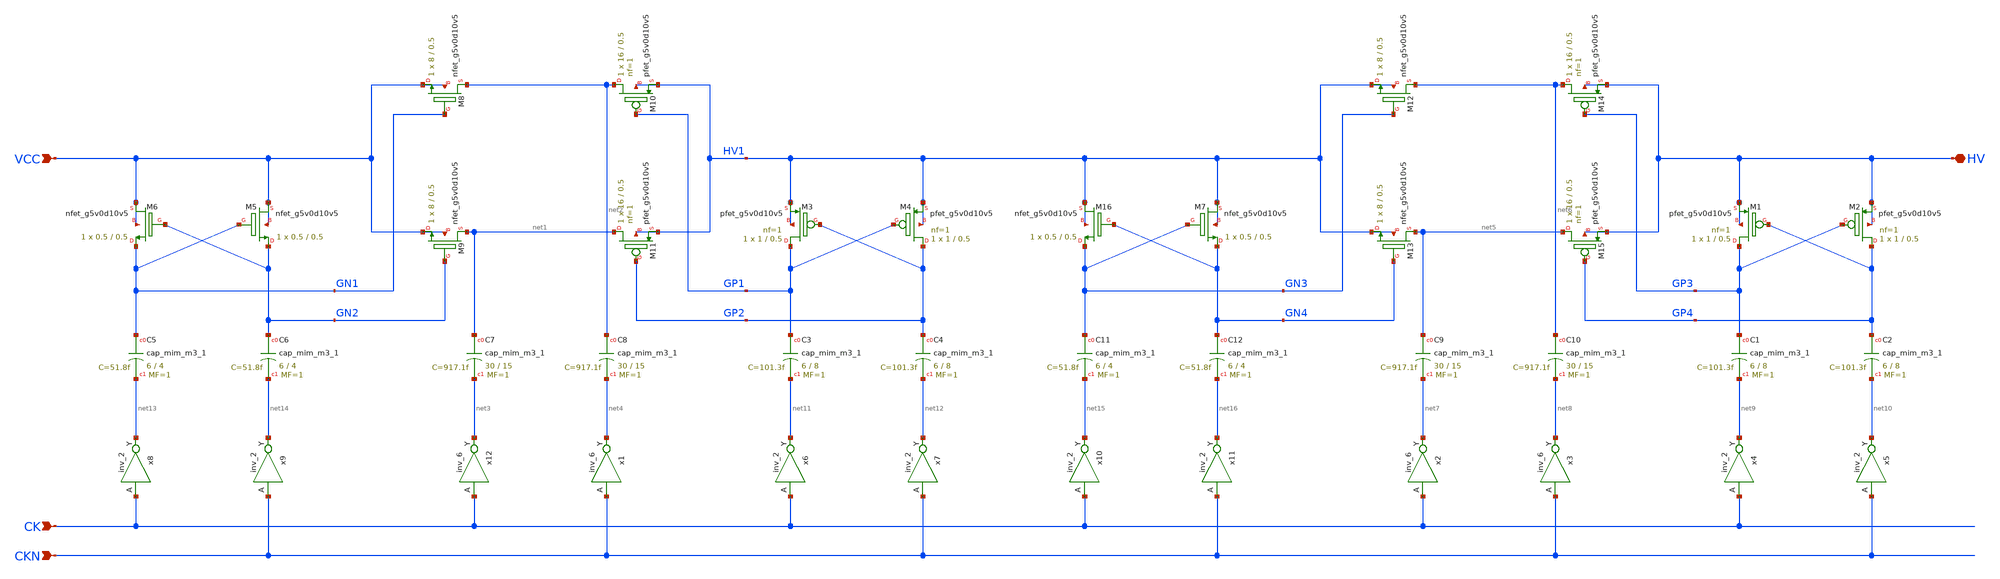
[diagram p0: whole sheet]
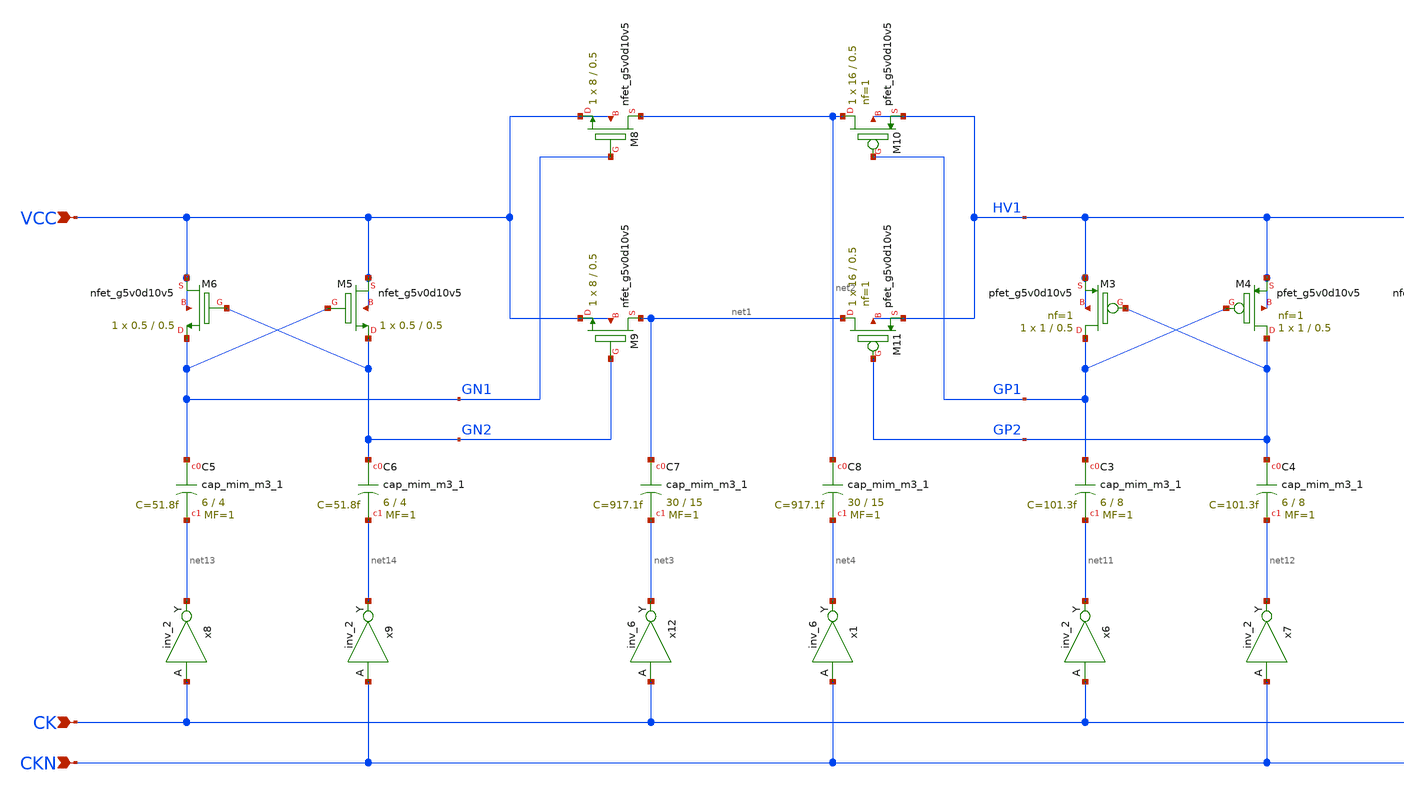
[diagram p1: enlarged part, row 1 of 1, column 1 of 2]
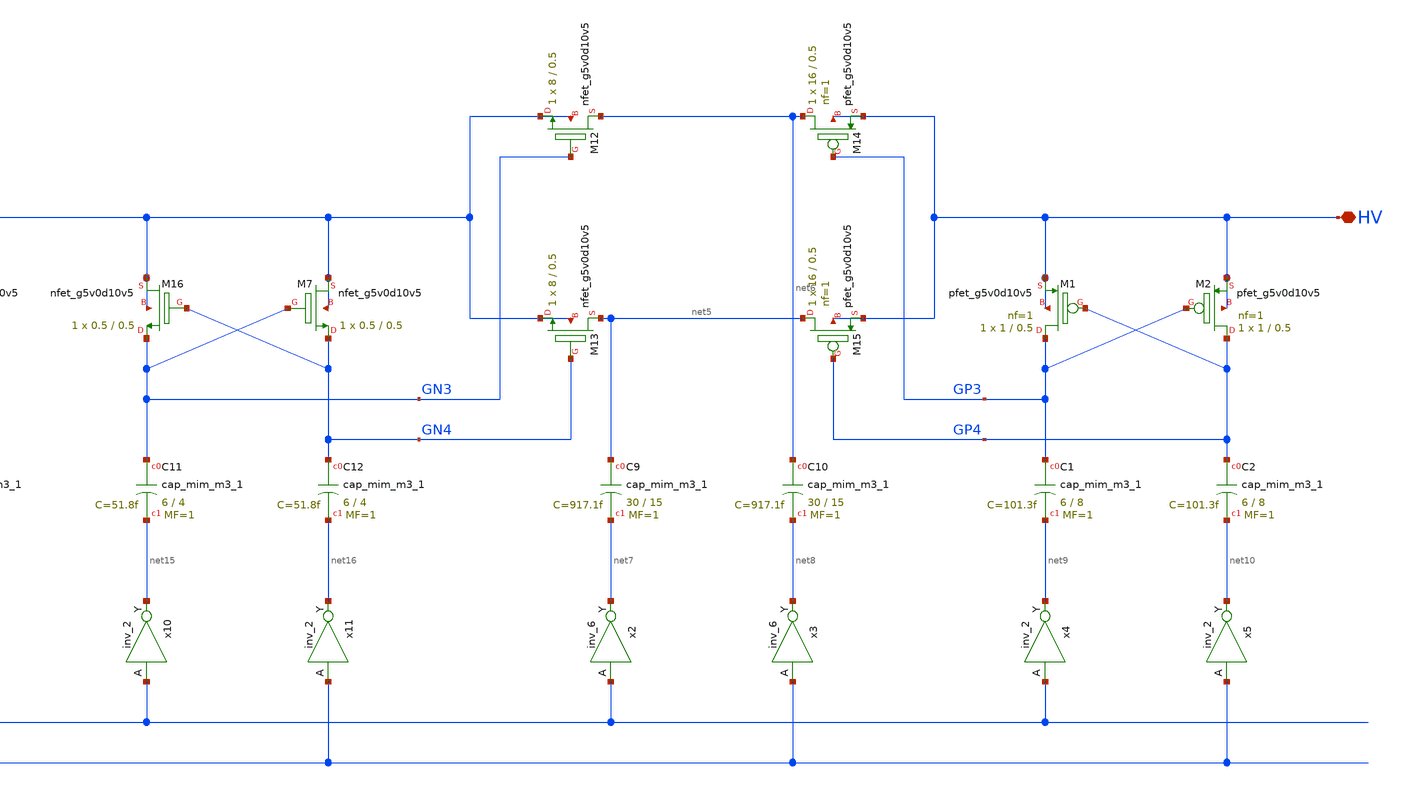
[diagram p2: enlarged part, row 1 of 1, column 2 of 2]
** sch_path: sky130_tests/charge_pump2.sch
* Copyright 2021 Stefan Frederik Schippers
* Licensed under the Apache License, Version 2.0 (the "License");
* you may not use this file except in compliance with the License.
* You may obtain a copy of the License at
* https://www.apache.org/licenses/LICENSE-2.0
* Unless required by applicable law or agreed to in writing, software
* distributed under the License is distributed on an "AS IS" BASIS,
* WITHOUT WARRANTIES OR CONDITIONS OF ANY KIND, either express or implied.
* See the License for the specific language governing permissions and
* limitations under the License.
**.subckt charge_pump2 VCC HV CK CKN
*.ipin VCC
*.iopin HV
*.ipin CK
*.ipin CKN
XM8 net2 GN1 VCC VCC sky130_fd_pr__nfet_g5v0d10v5 W=8 L=0.5 ad='int((nf+1)/2) * W/nf * 0.29' pd='2*int((nf+1)/2) * (W/nf + 0.29)'
+ as='int((nf+2)/2) * W/nf * 0.29' ps='2*int((nf+2)/2) * (W/nf + 0.29)' nrd='0.29 / W' nrs='0.29 / W' sa=0
+ sb=0 sd=0 nf=1 mult=1
XM9 net1 GN2 VCC VCC sky130_fd_pr__nfet_g5v0d10v5 W=8 L=0.5 ad='int((nf+1)/2) * W/nf * 0.29' pd='2*int((nf+1)/2) * (W/nf + 0.29)'
+ as='int((nf+2)/2) * W/nf * 0.29' ps='2*int((nf+2)/2) * (W/nf + 0.29)' nrd='0.29 / W' nrs='0.29 / W' sa=0
+ sb=0 sd=0 nf=1 mult=1
XM10 net2 GP1 HV1 HV1 sky130_fd_pr__pfet_g5v0d10v5 L=0.5 W=16 nf=1 ad='int((nf+1)/2) * W/nf * 0.29' as='int((nf+2)/2) * W/nf * 0.29'
+ pd='2*int((nf+1)/2) * (W/nf + 0.29)' ps='2*int((nf+2)/2) * (W/nf + 0.29)' nrd='0.29 / W' nrs='0.29 / W'
+ sa=0 sb=0 sd=0 mult=1 m=1
XM11 net1 GP2 HV1 HV1 sky130_fd_pr__pfet_g5v0d10v5 L=0.5 W=16 nf=1 ad='int((nf+1)/2) * W/nf * 0.29' as='int((nf+2)/2) * W/nf * 0.29'
+ pd='2*int((nf+1)/2) * (W/nf + 0.29)' ps='2*int((nf+2)/2) * (W/nf + 0.29)' nrd='0.29 / W' nrs='0.29 / W'
+ sa=0 sb=0 sd=0 mult=1 m=1
XC7 net1 net3 sky130_fd_pr__cap_mim_m3_1 W=30 L=15 MF=1 m=1
XC8 net2 net4 sky130_fd_pr__cap_mim_m3_1 W=30 L=15 MF=1 m=1
XM12 net6 GN3 HV1 HV1 sky130_fd_pr__nfet_g5v0d10v5 W=8 L=0.5 ad='int((nf+1)/2) * W/nf * 0.29' pd='2*int((nf+1)/2) * (W/nf + 0.29)'
+ as='int((nf+2)/2) * W/nf * 0.29' ps='2*int((nf+2)/2) * (W/nf + 0.29)' nrd='0.29 / W' nrs='0.29 / W' sa=0
+ sb=0 sd=0 nf=1 mult=1
XM13 net5 GN4 HV1 HV1 sky130_fd_pr__nfet_g5v0d10v5 W=8 L=0.5 ad='int((nf+1)/2) * W/nf * 0.29' pd='2*int((nf+1)/2) * (W/nf + 0.29)'
+ as='int((nf+2)/2) * W/nf * 0.29' ps='2*int((nf+2)/2) * (W/nf + 0.29)' nrd='0.29 / W' nrs='0.29 / W' sa=0
+ sb=0 sd=0 nf=1 mult=1
XM14 net6 GP3 HV HV sky130_fd_pr__pfet_g5v0d10v5 L=0.5 W=16 nf=1 ad='int((nf+1)/2) * W/nf * 0.29' as='int((nf+2)/2) * W/nf * 0.29'
+ pd='2*int((nf+1)/2) * (W/nf + 0.29)' ps='2*int((nf+2)/2) * (W/nf + 0.29)' nrd='0.29 / W' nrs='0.29 / W'
+ sa=0 sb=0 sd=0 mult=1 m=1
XM15 net5 GP4 HV HV sky130_fd_pr__pfet_g5v0d10v5 L=0.5 W=16 nf=1 ad='int((nf+1)/2) * W/nf * 0.29' as='int((nf+2)/2) * W/nf * 0.29'
+ pd='2*int((nf+1)/2) * (W/nf + 0.29)' ps='2*int((nf+2)/2) * (W/nf + 0.29)' nrd='0.29 / W' nrs='0.29 / W'
+ sa=0 sb=0 sd=0 mult=1 m=1
XC9 net5 net7 sky130_fd_pr__cap_mim_m3_1 W=30 L=15 MF=1 m=1
XC10 net6 net8 sky130_fd_pr__cap_mim_m3_1 W=30 L=15 MF=1 m=1
x12 CK GND GND VCC VCC net3 sky130_fd_sc_hd__inv_6
x1 CKN GND GND VCC VCC net4 sky130_fd_sc_hd__inv_6
x2 CK GND GND VCC VCC net7 sky130_fd_sc_hd__inv_6
x3 CKN GND GND VCC VCC net8 sky130_fd_sc_hd__inv_6
XM1 GP3 GP4 HV HV sky130_fd_pr__pfet_g5v0d10v5 L=0.5 W=1 nf=1 ad='int((nf+1)/2) * W/nf * 0.29' as='int((nf+2)/2) * W/nf * 0.29'
+ pd='2*int((nf+1)/2) * (W/nf + 0.29)' ps='2*int((nf+2)/2) * (W/nf + 0.29)' nrd='0.29 / W' nrs='0.29 / W'
+ sa=0 sb=0 sd=0 mult=1 m=1
XM2 GP4 GP3 HV HV sky130_fd_pr__pfet_g5v0d10v5 L=0.5 W=1 nf=1 ad='int((nf+1)/2) * W/nf * 0.29' as='int((nf+2)/2) * W/nf * 0.29'
+ pd='2*int((nf+1)/2) * (W/nf + 0.29)' ps='2*int((nf+2)/2) * (W/nf + 0.29)' nrd='0.29 / W' nrs='0.29 / W'
+ sa=0 sb=0 sd=0 mult=1 m=1
XC1 GP3 net9 sky130_fd_pr__cap_mim_m3_1 W=6 L=8 MF=1 m=1
XC2 GP4 net10 sky130_fd_pr__cap_mim_m3_1 W=6 L=8 MF=1 m=1
XM3 GP1 GP2 HV1 HV1 sky130_fd_pr__pfet_g5v0d10v5 L=0.5 W=1 nf=1 ad='int((nf+1)/2) * W/nf * 0.29' as='int((nf+2)/2) * W/nf * 0.29'
+ pd='2*int((nf+1)/2) * (W/nf + 0.29)' ps='2*int((nf+2)/2) * (W/nf + 0.29)' nrd='0.29 / W' nrs='0.29 / W'
+ sa=0 sb=0 sd=0 mult=1 m=1
XM4 GP2 GP1 HV1 HV1 sky130_fd_pr__pfet_g5v0d10v5 L=0.5 W=1 nf=1 ad='int((nf+1)/2) * W/nf * 0.29' as='int((nf+2)/2) * W/nf * 0.29'
+ pd='2*int((nf+1)/2) * (W/nf + 0.29)' ps='2*int((nf+2)/2) * (W/nf + 0.29)' nrd='0.29 / W' nrs='0.29 / W'
+ sa=0 sb=0 sd=0 mult=1 m=1
XC3 GP1 net11 sky130_fd_pr__cap_mim_m3_1 W=6 L=8 MF=1 m=1
XC4 GP2 net12 sky130_fd_pr__cap_mim_m3_1 W=6 L=8 MF=1 m=1
x4 CK GND GND VCC VCC net9 sky130_fd_sc_hd__inv_2
x5 CKN GND GND VCC VCC net10 sky130_fd_sc_hd__inv_2
x6 CK GND GND VCC VCC net11 sky130_fd_sc_hd__inv_2
x7 CKN GND GND VCC VCC net12 sky130_fd_sc_hd__inv_2
XC5 GN1 net13 sky130_fd_pr__cap_mim_m3_1 W=6 L=4 MF=1 m=1
XC6 GN2 net14 sky130_fd_pr__cap_mim_m3_1 W=6 L=4 MF=1 m=1
x8 CK GND GND VCC VCC net13 sky130_fd_sc_hd__inv_2
x9 CKN GND GND VCC VCC net14 sky130_fd_sc_hd__inv_2
XM5 VCC GN1 GN2 VCC sky130_fd_pr__nfet_g5v0d10v5 W=0.5 L=0.5 ad='int((nf+1)/2) * W/nf * 0.29' pd='2*int((nf+1)/2) * (W/nf + 0.29)'
+ as='int((nf+2)/2) * W/nf * 0.29' ps='2*int((nf+2)/2) * (W/nf + 0.29)' nrd='0.29 / W' nrs='0.29 / W' sa=0
+ sb=0 sd=0 nf=1 mult=1
XM6 VCC GN2 GN1 VCC sky130_fd_pr__nfet_g5v0d10v5 W=0.5 L=0.5 ad='int((nf+1)/2) * W/nf * 0.29' pd='2*int((nf+1)/2) * (W/nf + 0.29)'
+ as='int((nf+2)/2) * W/nf * 0.29' ps='2*int((nf+2)/2) * (W/nf + 0.29)' nrd='0.29 / W' nrs='0.29 / W' sa=0
+ sb=0 sd=0 nf=1 mult=1
XC11 GN3 net15 sky130_fd_pr__cap_mim_m3_1 W=6 L=4 MF=1 m=1
XC12 GN4 net16 sky130_fd_pr__cap_mim_m3_1 W=6 L=4 MF=1 m=1
x10 CK GND GND VCC VCC net15 sky130_fd_sc_hd__inv_2
x11 CKN GND GND VCC VCC net16 sky130_fd_sc_hd__inv_2
XM7 HV1 GN3 GN4 HV1 sky130_fd_pr__nfet_g5v0d10v5 W=0.5 L=0.5 ad='int((nf+1)/2) * W/nf * 0.29' pd='2*int((nf+1)/2) * (W/nf + 0.29)'
+ as='int((nf+2)/2) * W/nf * 0.29' ps='2*int((nf+2)/2) * (W/nf + 0.29)' nrd='0.29 / W' nrs='0.29 / W' sa=0
+ sb=0 sd=0 nf=1 mult=1
XM16 HV1 GN4 GN3 HV1 sky130_fd_pr__nfet_g5v0d10v5 W=0.5 L=0.5 ad='int((nf+1)/2) * W/nf * 0.29' pd='2*int((nf+1)/2) * (W/nf + 0.29)'
+ as='int((nf+2)/2) * W/nf * 0.29' ps='2*int((nf+2)/2) * (W/nf + 0.29)' nrd='0.29 / W' nrs='0.29 / W' sa=0
+ sb=0 sd=0 nf=1 mult=1
**.ends
.end
